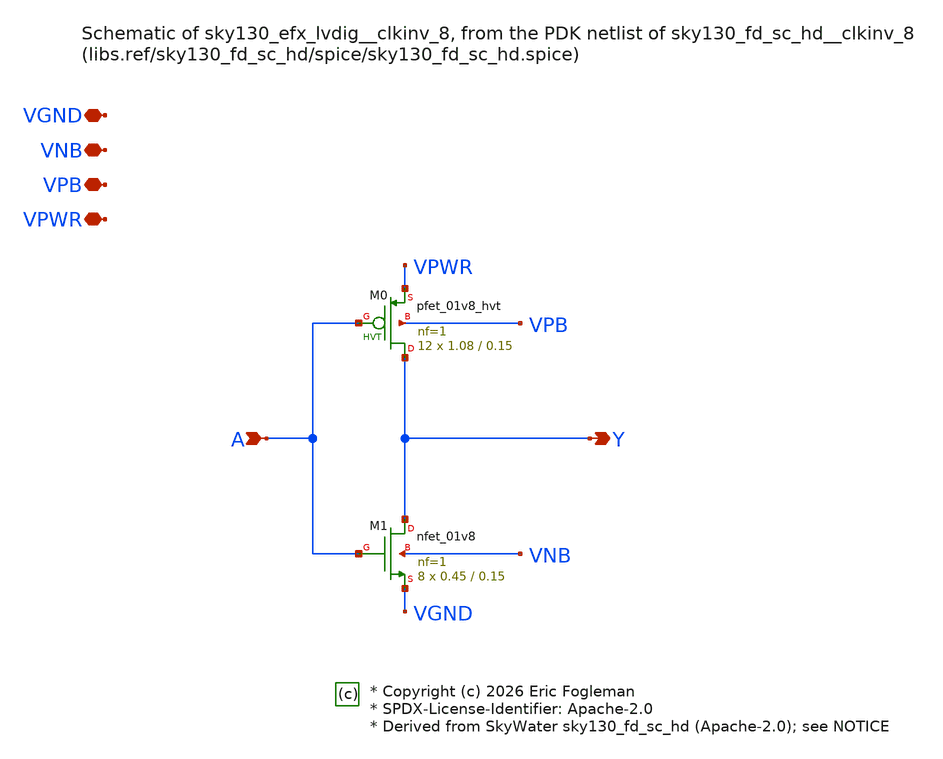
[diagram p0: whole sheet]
** sch_path: xschem/sky130_efx_lvdig__clkinv_8.sch

* Copyright (c) 2026 Eric Fogleman
* SPDX-License-Identifier: Apache-2.0
* Derived from SkyWater sky130_fd_sc_hd (Apache-2.0); see NOTICE

**.subckt sky130_efx_lvdig__clkinv_8 A Y VGND VNB VPB VPWR
*.ipin A
*.opin Y
*.iopin VGND
*.iopin VNB
*.iopin VPB
*.iopin VPWR
XM0 Y A VPWR VPB sky130_fd_pr__pfet_01v8_hvt L=0.15 W=1.08 nf=1 ad='int((1 + 1)/2) * 1.08 / 1 * 0.29'
+ as='int((1 + 2)/2) * 1.08 / 1 * 0.29' pd='2*int((1 + 1)/2) * (1.08 / 1 + 0.29)' ps='2*int((1 + 2)/2) * (1.08 / 1 + 0.29)'
+ nrd='0.29 / 1.08 ' nrs='0.29 / 1.08 ' sa=0 sb=0 sd=0 mult=12 m=12
XM1 Y A VGND VNB sky130_fd_pr__nfet_01v8 L=0.15 W=0.45 nf=1 ad='int((1 + 1)/2) * 0.45 / 1 * 0.29' as='int((1 + 2)/2) * 0.45 / 1 * 0.29'
+ pd='2*int((1 + 1)/2) * (0.45 / 1 + 0.29)' ps='2*int((1 + 2)/2) * (0.45 / 1 + 0.29)' nrd='0.29 / 0.45 '
+ nrs='0.29 / 0.45 ' sa=0 sb=0 sd=0 mult=8 m=8
**.ends
.end
